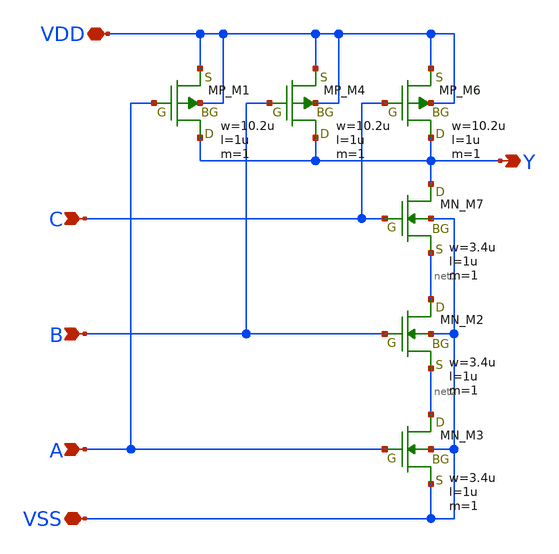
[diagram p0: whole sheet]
** sch_path: member_project/imager/YuMaehashi/design/pulsegen_nand3.sch
**.subckt pulsegen_nand3 B A Y VSS VDD C
*.ipin B
*.ipin A
*.opin Y
*.iopin VSS
*.iopin VDD
*.ipin C
XM1 Y A VDD VDD PMOS w=10.2u l=1u as=0 ad=0 ps=0 pd=0 nrd=0 nrs=0 m=1
XM4 Y B VDD VDD PMOS w=10.2u l=1u as=0 ad=0 ps=0 pd=0 nrd=0 nrs=0 m=1
XM6 Y C VDD VDD PMOS w=10.2u l=1u as=0 ad=0 ps=0 pd=0 nrd=0 nrs=0 m=1
XM7 Y C net1 VSS NMOS w=3.4u l=1u as=0 ad=0 ps=0 pd=0 nrd=0 nrs=0 m=1
XM2 net1 B net2 VSS NMOS w=3.4u l=1u as=0 ad=0 ps=0 pd=0 nrd=0 nrs=0 m=1
XM3 net2 A VSS VSS NMOS w=3.4u l=1u as=0 ad=0 ps=0 pd=0 nrd=0 nrs=0 m=1
**.ends
.end
